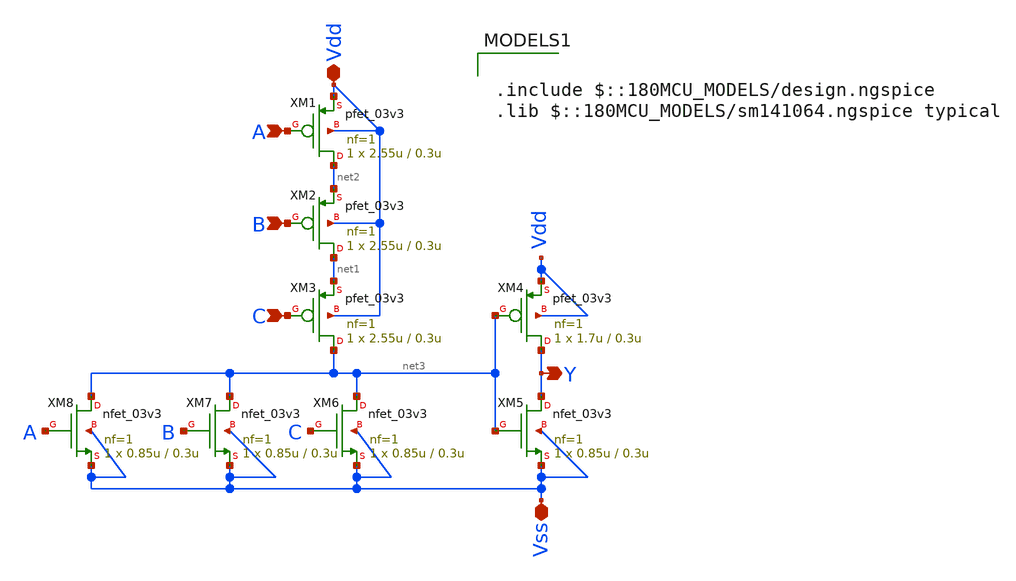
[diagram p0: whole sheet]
** sch_path: Cells/OR3_1/or3_1.sch
**.subckt or3_1 Vdd A B C Y Vss
*.iopin Vdd
*.ipin A
*.ipin B
*.ipin C
*.opin Y
*.iopin Vss
XM1 net2 A Vdd Vdd pfet_03v3 L=0.3u W=2.55u nf=1 ad='int((nf+1)/2) * W/nf * 0.18u' as='int((nf+2)/2) * W/nf * 0.18u'
+ pd='2*int((nf+1)/2) * (W/nf + 0.18u)' ps='2*int((nf+2)/2) * (W/nf + 0.18u)' nrd='0.18u / W' nrs='0.18u / W'
+ sa=0 sb=0 sd=0 m=1
XM2 net1 B net2 Vdd pfet_03v3 L=0.3u W=2.55u nf=1 ad='int((nf+1)/2) * W/nf * 0.18u' as='int((nf+2)/2) * W/nf * 0.18u'
+ pd='2*int((nf+1)/2) * (W/nf + 0.18u)' ps='2*int((nf+2)/2) * (W/nf + 0.18u)' nrd='0.18u / W' nrs='0.18u / W'
+ sa=0 sb=0 sd=0 m=1
XM3 net3 C net1 Vdd pfet_03v3 L=0.3u W=2.55u nf=1 ad='int((nf+1)/2) * W/nf * 0.18u' as='int((nf+2)/2) * W/nf * 0.18u'
+ pd='2*int((nf+1)/2) * (W/nf + 0.18u)' ps='2*int((nf+2)/2) * (W/nf + 0.18u)' nrd='0.18u / W' nrs='0.18u / W'
+ sa=0 sb=0 sd=0 m=1
XM4 Y net3 Vdd Vdd pfet_03v3 L=0.3u W=1.7u nf=1 ad='int((nf+1)/2) * W/nf * 0.18u' as='int((nf+2)/2) * W/nf * 0.18u'
+ pd='2*int((nf+1)/2) * (W/nf + 0.18u)' ps='2*int((nf+2)/2) * (W/nf + 0.18u)' nrd='0.18u / W' nrs='0.18u / W'
+ sa=0 sb=0 sd=0 m=1
XM5 Y net3 Vss Vss nfet_03v3 L=0.3u W=0.85u nf=1 ad='int((nf+1)/2) * W/nf * 0.18u' as='int((nf+2)/2) * W/nf * 0.18u'
+ pd='2*int((nf+1)/2) * (W/nf + 0.18u)' ps='2*int((nf+2)/2) * (W/nf + 0.18u)' nrd='0.18u / W' nrs='0.18u / W'
+ sa=0 sb=0 sd=0 m=1
XM6 net3 C Vss Vss nfet_03v3 L=0.3u W=0.85u nf=1 ad='int((nf+1)/2) * W/nf * 0.18u' as='int((nf+2)/2) * W/nf * 0.18u'
+ pd='2*int((nf+1)/2) * (W/nf + 0.18u)' ps='2*int((nf+2)/2) * (W/nf + 0.18u)' nrd='0.18u / W' nrs='0.18u / W'
+ sa=0 sb=0 sd=0 m=1
XM7 net3 B Vss Vss nfet_03v3 L=0.3u W=0.85u nf=1 ad='int((nf+1)/2) * W/nf * 0.18u' as='int((nf+2)/2) * W/nf * 0.18u'
+ pd='2*int((nf+1)/2) * (W/nf + 0.18u)' ps='2*int((nf+2)/2) * (W/nf + 0.18u)' nrd='0.18u / W' nrs='0.18u / W'
+ sa=0 sb=0 sd=0 m=1
XM8 net3 A Vss Vss nfet_03v3 L=0.3u W=0.85u nf=1 ad='int((nf+1)/2) * W/nf * 0.18u' as='int((nf+2)/2) * W/nf * 0.18u'
+ pd='2*int((nf+1)/2) * (W/nf + 0.18u)' ps='2*int((nf+2)/2) * (W/nf + 0.18u)' nrd='0.18u / W' nrs='0.18u / W'
+ sa=0 sb=0 sd=0 m=1
**** begin user architecture code

.include $::180MCU_MODELS/design.ngspice
.lib $::180MCU_MODELS/sm141064.ngspice typical

**** end user architecture code
**.ends
.end
